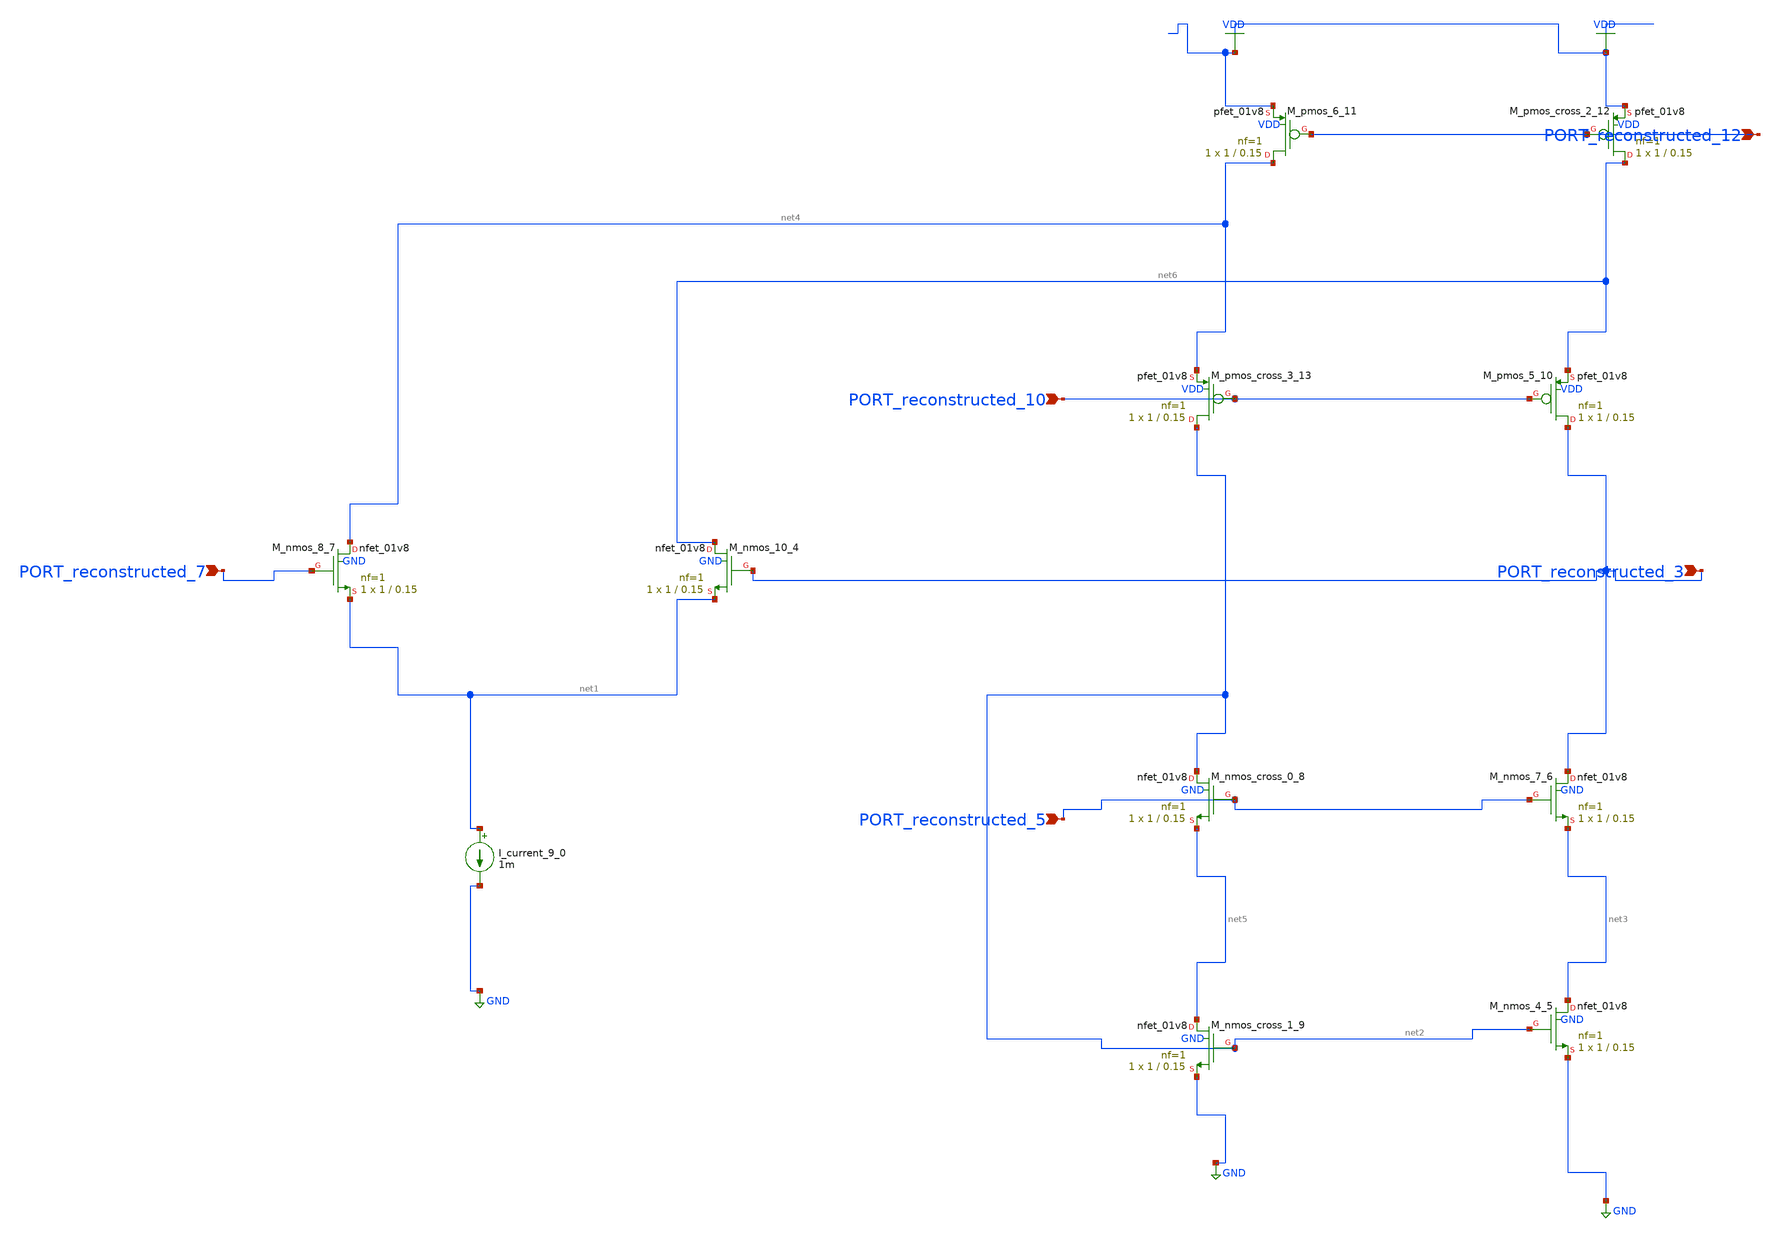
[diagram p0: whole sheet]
** sch_path: schematics/AMSNet/683.sch
**.subckt 683 PORT_reconstructed_3 PORT_reconstructed_7 PORT_reconstructed_5 PORT_reconstructed_10
*+ PORT_reconstructed_12
*.ipin PORT_reconstructed_3
*.ipin PORT_reconstructed_7
*.ipin PORT_reconstructed_5
*.ipin PORT_reconstructed_10
*.ipin PORT_reconstructed_12
I_current_9_0 net1 GND 1m
XM_nmos_10_4 net6 PORT_reconstructed_3 net1 GND sky130_fd_pr__nfet_01v8 L=0.15 W=1 nf=1 ad='int((1 + 1)/2) * 1 / 1 * 0.29'
+ as='int((1 + 2)/2) * 1 / 1 * 0.29' pd='2*int((1 + 1)/2) * (1 / 1 + 0.29)' ps='2*int((1 + 2)/2) * (1 / 1 + 0.29)'
+ nrd='0.29 / 1 ' nrs='0.29 / 1 ' sa=0 sb=0 sd=0 mult=1 m=1
XM_nmos_4_5 net3 net2 GND GND sky130_fd_pr__nfet_01v8 L=0.15 W=1 nf=1 ad='int((1 + 1)/2) * 1 / 1 * 0.29'
+ as='int((1 + 2)/2) * 1 / 1 * 0.29' pd='2*int((1 + 1)/2) * (1 / 1 + 0.29)' ps='2*int((1 + 2)/2) * (1 / 1 + 0.29)'
+ nrd='0.29 / 1 ' nrs='0.29 / 1 ' sa=0 sb=0 sd=0 mult=1 m=1
XM_nmos_7_6 PORT_reconstructed_3 PORT_reconstructed_5 net3 GND sky130_fd_pr__nfet_01v8 L=0.15 W=1 nf=1
+ ad='int((1 + 1)/2) * 1 / 1 * 0.29' as='int((1 + 2)/2) * 1 / 1 * 0.29' pd='2*int((1 + 1)/2) * (1 / 1 + 0.29)'
+ ps='2*int((1 + 2)/2) * (1 / 1 + 0.29)' nrd='0.29 / 1 ' nrs='0.29 / 1 ' sa=0 sb=0 sd=0 mult=1 m=1
XM_nmos_8_7 net4 PORT_reconstructed_7 net1 GND sky130_fd_pr__nfet_01v8 L=0.15 W=1 nf=1 ad='int((1 + 1)/2) * 1 / 1 * 0.29'
+ as='int((1 + 2)/2) * 1 / 1 * 0.29' pd='2*int((1 + 1)/2) * (1 / 1 + 0.29)' ps='2*int((1 + 2)/2) * (1 / 1 + 0.29)'
+ nrd='0.29 / 1 ' nrs='0.29 / 1 ' sa=0 sb=0 sd=0 mult=1 m=1
XM_nmos_cross_0_8 net2 PORT_reconstructed_5 net5 GND sky130_fd_pr__nfet_01v8 L=0.15 W=1 nf=1 ad='int((1 + 1)/2) * 1 / 1 * 0.29'
+ as='int((1 + 2)/2) * 1 / 1 * 0.29' pd='2*int((1 + 1)/2) * (1 / 1 + 0.29)' ps='2*int((1 + 2)/2) * (1 / 1 + 0.29)'
+ nrd='0.29 / 1 ' nrs='0.29 / 1 ' sa=0 sb=0 sd=0 mult=1 m=1
XM_nmos_cross_1_9 net5 net2 GND GND sky130_fd_pr__nfet_01v8 L=0.15 W=1 nf=1 ad='int((1 + 1)/2) * 1 / 1 * 0.29'
+ as='int((1 + 2)/2) * 1 / 1 * 0.29' pd='2*int((1 + 1)/2) * (1 / 1 + 0.29)' ps='2*int((1 + 2)/2) * (1 / 1 + 0.29)'
+ nrd='0.29 / 1 ' nrs='0.29 / 1 ' sa=0 sb=0 sd=0 mult=1 m=1
XM_pmos_5_10 PORT_reconstructed_3 PORT_reconstructed_10 net6 VDD sky130_fd_pr__pfet_01v8 L=0.15 W=1 nf=1
+ ad='int((1 + 1)/2) * 1 / 1 * 0.29' as='int((1 + 2)/2) * 1 / 1 * 0.29' pd='2*int((1 + 1)/2) * (1 / 1 + 0.29)'
+ ps='2*int((1 + 2)/2) * (1 / 1 + 0.29)' nrd='0.29 / 1 ' nrs='0.29 / 1 ' sa=0 sb=0 sd=0 mult=1 m=1
XM_pmos_6_11 net4 PORT_reconstructed_12 VDD VDD sky130_fd_pr__pfet_01v8 L=0.15 W=1 nf=1 ad='int((1 + 1)/2) * 1 / 1 * 0.29'
+ as='int((1 + 2)/2) * 1 / 1 * 0.29' pd='2*int((1 + 1)/2) * (1 / 1 + 0.29)' ps='2*int((1 + 2)/2) * (1 / 1 + 0.29)'
+ nrd='0.29 / 1 ' nrs='0.29 / 1 ' sa=0 sb=0 sd=0 mult=1 m=1
XM_pmos_cross_2_12 net6 PORT_reconstructed_12 VDD VDD sky130_fd_pr__pfet_01v8 L=0.15 W=1 nf=1 ad='int((1 + 1)/2) * 1 / 1 * 0.29'
+ as='int((1 + 2)/2) * 1 / 1 * 0.29' pd='2*int((1 + 1)/2) * (1 / 1 + 0.29)' ps='2*int((1 + 2)/2) * (1 / 1 + 0.29)'
+ nrd='0.29 / 1 ' nrs='0.29 / 1 ' sa=0 sb=0 sd=0 mult=1 m=1
XM_pmos_cross_3_13 net2 PORT_reconstructed_10 net4 VDD sky130_fd_pr__pfet_01v8 L=0.15 W=1 nf=1 ad='int((1 + 1)/2) * 1 / 1 * 0.29'
+ as='int((1 + 2)/2) * 1 / 1 * 0.29' pd='2*int((1 + 1)/2) * (1 / 1 + 0.29)' ps='2*int((1 + 2)/2) * (1 / 1 + 0.29)'
+ nrd='0.29 / 1 ' nrs='0.29 / 1 ' sa=0 sb=0 sd=0 mult=1 m=1
**.ends
.GLOBAL GND
.GLOBAL VDD
.end
